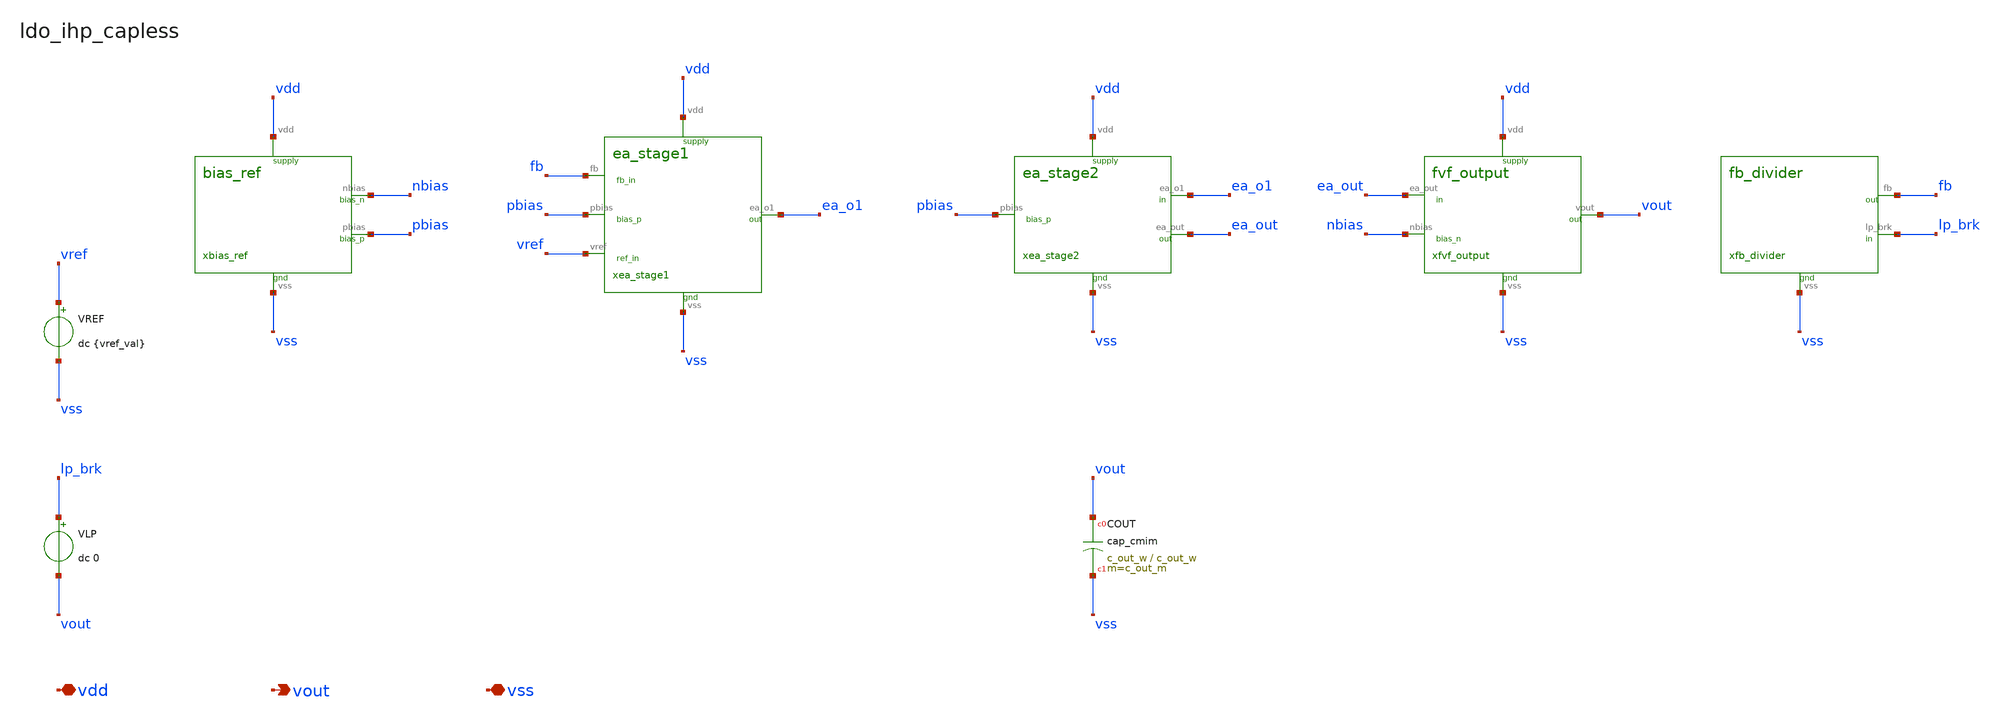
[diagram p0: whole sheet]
** sch_path: analog-db/circuits/ldo_010_capless_lowiq/pdk/ihp-sg13g2/schematic/ldo_ihp_capless.sch
**.subckt ldo_ihp_capless vdd vout vss
*.iopin vdd
*.opin vout
*.iopin vss
xbias_ref nbias pbias vdd vss bias_ref
xea_stage1 fb pbias vref ea_o1 vdd vss ea_stage1
xea_stage2 pbias ea_o1 ea_out vdd vss ea_stage2
xfvf_output ea_out nbias vout vdd vss fvf_output
xfb_divider fb lp_brk vss fb_divider
VREF vref vss dc {vref_val}
VLP lp_brk vout dc 0
XCOUT vout vss cap_cmim w=c_out_w l=c_out_w m=c_out_m
**.ends

* expanding   symbol:  blocks/bias_ref.sym # of pins=4
** sym_path: analog-db/circuits/ldo_010_capless_lowiq/pdk/ihp-sg13g2/schematic/blocks/bias_ref.sym
** sch_path: analog-db/circuits/ldo_010_capless_lowiq/pdk/ihp-sg13g2/schematic/blocks/bias_ref.sch
.subckt bias_ref nbias pbias vdd vss
*.opin nbias
*.opin pbias
*.iopin vdd
*.iopin vss
XRB_1 vdd n_rb_1 vss rhigh w=r_w l={r_bias_l/5} m=1 b=0
XRB_2 n_rb_1 n_rb_2 vss rhigh w=r_w l={r_bias_l/5} m=1 b=0
XRB_3 n_rb_2 n_rb_3 vss rhigh w=r_w l={r_bias_l/5} m=1 b=0
XRB_4 n_rb_3 n_rb_4 vss rhigh w=r_w l={r_bias_l/5} m=1 b=0
XRB_5 n_rb_4 nbias vss rhigh w=r_w l={r_bias_l/5} m=1 b=0
XMB0A nbias nbias vss vss sg13_lv_nmos w={x_dut_xmb0_w/2} l=x_dut_xmb0_l ng=1 m=1 mm_ok=1
XMB0B nbias nbias vss vss sg13_lv_nmos w={x_dut_xmb0_w/2} l=x_dut_xmb0_l ng=1 m=1 mm_ok=1
XMB1A pbias nbias vss vss sg13_lv_nmos w={x_dut_xmb1_w/2} l=x_dut_xmb0_l ng=1 m=1 mm_ok=1
XMB1B pbias nbias vss vss sg13_lv_nmos w={x_dut_xmb1_w/2} l=x_dut_xmb0_l ng=1 m=1 mm_ok=1
XMBP pbias pbias vdd vdd sg13_lv_pmos w=x_dut_xmbp_w l=x_dut_xmbp_l ng=1 m=1 mm_ok=1
.ends


* expanding   symbol:  blocks/ea_stage1.sym # of pins=6
** sym_path: analog-db/circuits/ldo_010_capless_lowiq/pdk/ihp-sg13g2/schematic/blocks/ea_stage1.sym
** sch_path: analog-db/circuits/ldo_010_capless_lowiq/pdk/ihp-sg13g2/schematic/blocks/ea_stage1.sch
.subckt ea_stage1 fb pbias vref ea_o1 vdd vss
*.ipin fb
*.ipin pbias
*.ipin vref
*.opin ea_o1
*.iopin vdd
*.iopin vss
XMT ea_tail pbias vdd vdd sg13_lv_pmos w=x_dut_xmt_w l=x_dut_xmbp_l ng=1 m=1 mm_ok=1
XM1A ea_n fb ea_tail vdd sg13_lv_pmos w={x_dut_xm1_w/2} l=x_dut_xm1_l ng=1 m=1 mm_ok=1
XM1B ea_n fb ea_tail vdd sg13_lv_pmos w={x_dut_xm1_w/2} l=x_dut_xm1_l ng=1 m=1 mm_ok=1
XM2A ea_o1 vref ea_tail vdd sg13_lv_pmos w={x_dut_xm1_w/2} l=x_dut_xm1_l ng=1 m=1 mm_ok=1
XM2B ea_o1 vref ea_tail vdd sg13_lv_pmos w={x_dut_xm1_w/2} l=x_dut_xm1_l ng=1 m=1 mm_ok=1
XM3A ea_n ea_n vss vss sg13_lv_nmos w={x_dut_xm3_w/2} l=x_dut_xm3_l ng=1 m=1 mm_ok=1
XM3B ea_n ea_n vss vss sg13_lv_nmos w={x_dut_xm3_w/2} l=x_dut_xm3_l ng=1 m=1 mm_ok=1
XM4A ea_o1 ea_n vss vss sg13_lv_nmos w={x_dut_xm3_w/2} l=x_dut_xm3_l ng=1 m=1 mm_ok=1
XM4B ea_o1 ea_n vss vss sg13_lv_nmos w={x_dut_xm3_w/2} l=x_dut_xm3_l ng=1 m=1 mm_ok=1
.ends


* expanding   symbol:  blocks/ea_stage2.sym # of pins=5
** sym_path: analog-db/circuits/ldo_010_capless_lowiq/pdk/ihp-sg13g2/schematic/blocks/ea_stage2.sym
** sch_path: analog-db/circuits/ldo_010_capless_lowiq/pdk/ihp-sg13g2/schematic/blocks/ea_stage2.sch
.subckt ea_stage2 pbias ea_o1 ea_out vdd vss
*.ipin pbias
*.iopin vdd
*.iopin ea_o1
*.iopin vss
*.opin ea_out
XM5 ea_out ea_o1 vss vss sg13_lv_nmos w=x_dut_xm5_w l=x_dut_xm5_l ng=1 m=1 mm_ok=1
XM6 ea_out pbias vdd vdd sg13_lv_pmos w=x_dut_xm6_w l=x_dut_xmbp_l ng=1 m=1 mm_ok=1
XCC ea_out ea_o1 cap_cmim w=c_comp_w l=c_comp_w m=1
.ends


* expanding   symbol:  blocks/fvf_output.sym # of pins=5
** sym_path: analog-db/circuits/ldo_010_capless_lowiq/pdk/ihp-sg13g2/schematic/blocks/fvf_output.sym
** sch_path: analog-db/circuits/ldo_010_capless_lowiq/pdk/ihp-sg13g2/schematic/blocks/fvf_output.sch
.subckt fvf_output ea_out nbias vout vdd vss
*.ipin nbias
*.ipin ea_out
*.iopin vdd
*.iopin vss
*.opin vout
XMC x1 ea_out vout vdd sg13_lv_pmos w=x_dut_xmc_w l=x_dut_xmc_l ng=1 m=1 mm_ok=1
XMA x1 x1 vss vss sg13_lv_nmos w=x_dut_xma_w l=x_dut_xma_l ng=1 m=1 mm_ok=1
XMB y x1 vss vss sg13_lv_nmos w=x_dut_xma_w l=x_dut_xma_l ng=1 m=1 mm_ok=1
XMCP y y vdd vdd sg13_lv_pmos w=x_dut_xmcp_w l=x_dut_xmcp_l ng=1 m=1 mm_ok=1
XMD gate y vdd vdd sg13_lv_pmos w=x_dut_xmcp_w l=x_dut_xmcp_l ng=1 m=1 mm_ok=1
XMSA gate nbias vss vss sg13_lv_nmos w={x_dut_xms_w/2} l=x_dut_xms_l ng=1 m=1 mm_ok=1
XMSB gate nbias vss vss sg13_lv_nmos w={x_dut_xms_w/2} l=x_dut_xms_l ng=1 m=1 mm_ok=1
XMP vout gate vdd vdd sg13_lv_pmos w={x_dut_xmp_w/x_dut_xmp_nf_mult} l=x_dut_xmp_l ng=1 m={x_dut_xmp_m*x_dut_xmp_nf_mult}
+ mm_ok=1
.ends


* expanding   symbol:  blocks/fb_divider.sym # of pins=3
** sym_path: analog-db/circuits/ldo_010_capless_lowiq/pdk/ihp-sg13g2/schematic/blocks/fb_divider.sym
** sch_path: analog-db/circuits/ldo_010_capless_lowiq/pdk/ihp-sg13g2/schematic/blocks/fb_divider.sch
.subckt fb_divider fb lp_brk vss
*.iopin lp_brk
*.iopin fb
*.iopin vss
XR1_1 lp_brk n_r1_1 vss rhigh w=r_w l={r_fb_l/8} m=1 b=0
XR1_2 n_r1_1 n_r1_2 vss rhigh w=r_w l={r_fb_l/8} m=1 b=0
XR1_3 n_r1_2 n_r1_3 vss rhigh w=r_w l={r_fb_l/8} m=1 b=0
XR1_4 n_r1_3 n_r1_4 vss rhigh w=r_w l={r_fb_l/8} m=1 b=0
XR1_5 n_r1_4 n_r1_5 vss rhigh w=r_w l={r_fb_l/8} m=1 b=0
XR1_6 n_r1_5 n_r1_6 vss rhigh w=r_w l={r_fb_l/8} m=1 b=0
XR1_7 n_r1_6 n_r1_7 vss rhigh w=r_w l={r_fb_l/8} m=1 b=0
XR1_8 n_r1_7 fb vss rhigh w=r_w l={r_fb_l/8} m=1 b=0
XR2_1 fb n_r2_1 vss rhigh w=r_w l={r_fb_l/8} m=1 b=0
XR2_2 n_r2_1 n_r2_2 vss rhigh w=r_w l={r_fb_l/8} m=1 b=0
XR2_3 n_r2_2 n_r2_3 vss rhigh w=r_w l={r_fb_l/8} m=1 b=0
XR2_4 n_r2_3 n_r2_4 vss rhigh w=r_w l={r_fb_l/8} m=1 b=0
XR2_5 n_r2_4 n_r2_5 vss rhigh w=r_w l={r_fb_l/8} m=1 b=0
XR2_6 n_r2_5 n_r2_6 vss rhigh w=r_w l={r_fb_l/8} m=1 b=0
XR2_7 n_r2_6 n_r2_7 vss rhigh w=r_w l={r_fb_l/8} m=1 b=0
XR2_8 n_r2_7 vss vss rhigh w=r_w l={r_fb_l/8} m=1 b=0
XCFF lp_brk fb cap_cmim w=c_ff_w l=c_ff_w m=1
.ends

.end
